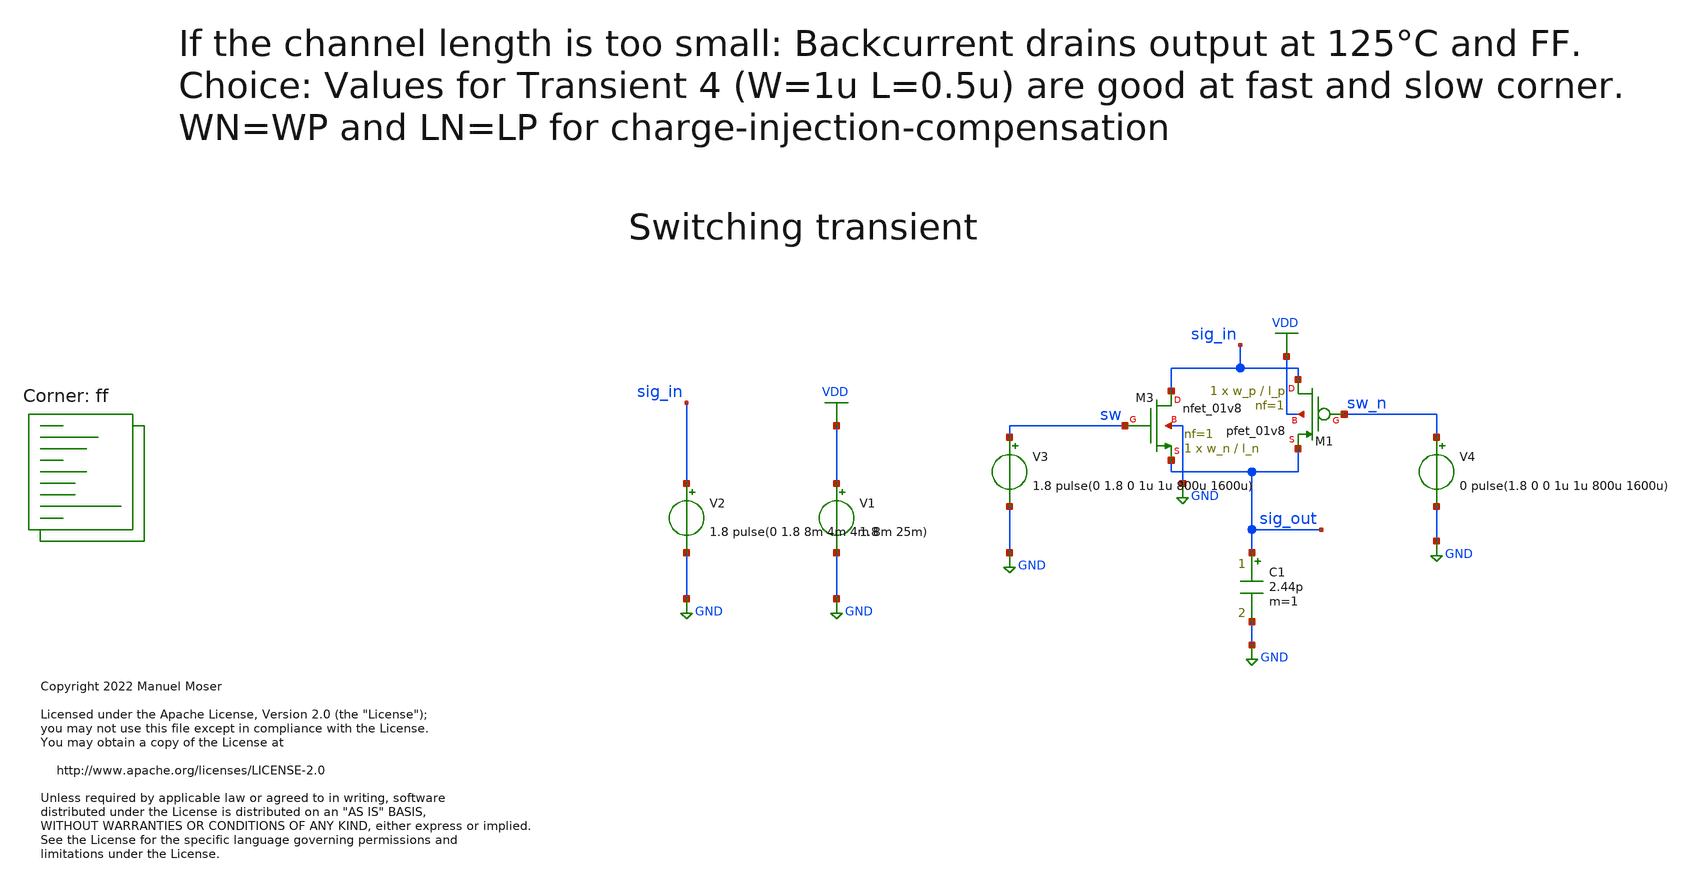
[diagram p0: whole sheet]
** sch_path: xschem/adc_vcm_switch_tb_transient.sch
* Copyright 2022 Manuel Moser
* Licensed under the Apache License, Version 2.0 (the "License");
**.subckt adc_vcm_switch_tb_transient
V1 VDD GND 1.8
V2 sig_in GND 1.8 pulse(0 1.8 8m 4m 4m 8m 25m)
V3 sw GND 1.8 pulse(0 1.8 0 1u 1u 800u 1600u)
V4 sw_n GND 0 pulse(1.8 0 0 1u 1u 800u 1600u)
C1 sig_out GND 2.44p m=1
XM1 sig_in sw_n sig_out VDD sky130_fd_pr__pfet_01v8 L=l_p W=w_p nf=1 ad='int((nf+1)/2) * W/nf * 0.29'
+ as='int((nf+2)/2) * W/nf * 0.29' pd='2*int((nf+1)/2) * (W/nf + 0.29)' ps='2*int((nf+2)/2) * (W/nf + 0.29)'
+ nrd='0.29 / W' nrs='0.29 / W' sa=0 sb=0 sd=0 mult=1 m=1
XM3 sig_in sw sig_out GND sky130_fd_pr__nfet_01v8 L=l_n W=w_n nf=1 ad='int((nf+1)/2) * W/nf * 0.29' as='int((nf+2)/2) * W/nf * 0.29'
+ pd='2*int((nf+1)/2) * (W/nf + 0.29)' ps='2*int((nf+2)/2) * (W/nf + 0.29)' nrd='0.29 / W' nrs='0.29 / W'
+ sa=0 sb=0 sd=0 mult=1 m=1
**** begin user architecture code
.lib $::SKYWATER_MODELS/sky130.lib.spice ff


.save all
.temp = 100
*.options method=gear
.OPTIONS savecurrents
.OPTIONS RELTOL=.1 TRTOL=1 ABSTOL=1e-20 CHGTOL=1.0e-20 DEFAD=1.0e-18
.save @m.x1.xm1.msky130_fd_pr__pfet_01v8[gm]
.save @m.x1.xm1.msky130_fd_pr__pfet_01v8[CGS]
.save @m.x1.xm1.msky130_fd_pr__pfet_01v8[Vth]
.save @m.x1.xm2.msky130_fd_pr__nfet_01v8_lvt[gm]
.save @m.x1.xm2.msky130_fd_pr__nfet_01v8_lvt[CGS]
.save @m.x1.xm2.msky130_fd_pr__nfet_01v8_lvt[Vth]


.param w_p=1
.param l_p = 1
.param w_n=1
.param l_n=1

.control
alterparam w_p=0.42
alterparam l_p=0.15
alterparam w_n=0.42
alterparam l_n=0.15
reset
tran 5u 40m 0 10u
write tran-sweep.out (-(v(sig2_in)-v(sig2_out))/I(v8)) (-(v(sig3_in)-v(sig3_out))/I(v7)) I(v7) I(v8)
set appendwrite


alterparam w_p=0.42
alterparam l_p=0.2
alterparam w_n=0.42
alterparam l_n=0.2
reset
tran 5u 40m 0 10u
write tran-sweep.out (-(v(sig2_in)-v(sig2_out))/I(v8)) (-(v(sig3_in)-v(sig3_out))/I(v7)) I(v7) I(v8)
set appendwrite


alterparam w_p=0.42
alterparam l_p=0.5
alterparam w_n=0.42
alterparam l_n=0.5
reset
tran 5u 40m 0 10u
write tran-sweep.out (-(v(sig2_in)-v(sig2_out))/I(v8)) (-(v(sig3_in)-v(sig3_out))/I(v7)) I(v7) I(v8)
set appendwrite

alterparam w_p=1
alterparam l_p=0.5
alterparam w_n=1
alterparam l_n=0.5
reset
tran 5u 40m 0 10u
write tran-sweep.out (-(v(sig2_in)-v(sig2_out))/I(v8)) (-(v(sig3_in)-v(sig3_out))/I(v7)) I(v7) I(v8)
set appendwrite

alterparam w_p=4
alterparam l_p=0.4
alterparam w_n=4
alterparam l_n=0.4
reset
tran 5u 40m 0 10u
write tran-sweep.out (-(v(sig2_in)-v(sig2_out))/I(v8)) (-(v(sig3_in)-v(sig3_out))/I(v7)) I(v7) I(v8)
set appendwrite


plot tran1.v(sig_in) tran1.v(sig_out) tran2.v(sig_out) tran3.v(sig_out) tran4.v(sig_out)
+ tran5.v(sig_out)
.endc


**** end user architecture code
**.ends
.GLOBAL GND
.GLOBAL VDD
.end
